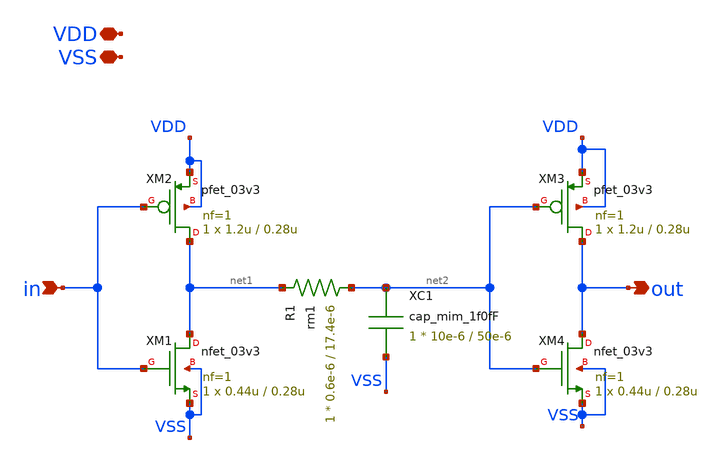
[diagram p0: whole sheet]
** sch_path: delay_buffer.sch
**.subckt delay_buffer in out VDD VSS
*.ipin in
*.opin out
*.iopin VDD
*.iopin VSS
XM1 net1 in VSS VSS nfet_03v3 L=0.28u W=0.44u nf=1 ad='int((nf+1)/2) * W/nf * 0.18u' as='int((nf+2)/2) * W/nf * 0.18u'
+ pd='2*int((nf+1)/2) * (W/nf + 0.18u)' ps='2*int((nf+2)/2) * (W/nf + 0.18u)' nrd='0.18u / W' nrs='0.18u / W'
+ sa=0 sb=0 sd=0 m=1
XM2 net1 in VDD VDD pfet_03v3 L=0.28u W=1.2u nf=1 ad='int((nf+1)/2) * W/nf * 0.18u' as='int((nf+2)/2) * W/nf * 0.18u'
+ pd='2*int((nf+1)/2) * (W/nf + 0.18u)' ps='2*int((nf+2)/2) * (W/nf + 0.18u)' nrd='0.18u / W' nrs='0.18u / W'
+ sa=0 sb=0 sd=0 m=1
XR1 net2 net1 rm1 r_width=0.6e-6 r_length=17.4e-6 m=1
XC1 net2 VSS cap_mim_1f0fF c_width=10e-6 c_length=50e-6 m=1
XM3 out net2 VDD VDD pfet_03v3 L=0.28u W=1.2u nf=1 ad='int((nf+1)/2) * W/nf * 0.18u' as='int((nf+2)/2) * W/nf * 0.18u'
+ pd='2*int((nf+1)/2) * (W/nf + 0.18u)' ps='2*int((nf+2)/2) * (W/nf + 0.18u)' nrd='0.18u / W' nrs='0.18u / W'
+ sa=0 sb=0 sd=0 m=1
XM4 out net2 VSS VSS nfet_03v3 L=0.28u W=0.44u nf=1 ad='int((nf+1)/2) * W/nf * 0.18u' as='int((nf+2)/2) * W/nf * 0.18u'
+ pd='2*int((nf+1)/2) * (W/nf + 0.18u)' ps='2*int((nf+2)/2) * (W/nf + 0.18u)' nrd='0.18u / W' nrs='0.18u / W'
+ sa=0 sb=0 sd=0 m=1
**.ends
.end
